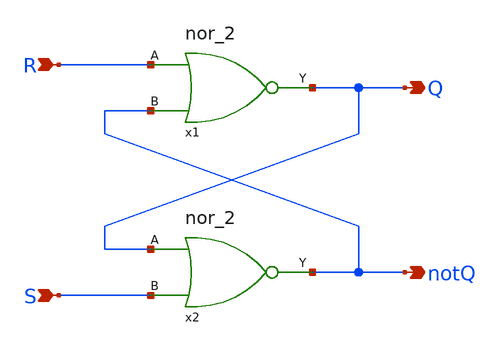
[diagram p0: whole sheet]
** sch_path: Circuiti/latches_sch_sym/sr_latch.sch
**.subckt sr_latch R S Q notQ
*.ipin R
*.ipin S
*.opin Q
*.opin notQ
x1 R Q notQ nor_2
x2 Q notQ S nor_2
**.ends

* expanding   symbol:  /home/matteo/Documenti/tesi/Circuiti/logic_gates_sch_sym/nor_2.sym # of
*+ pins=3
** sym_path: Circuiti/logic_gates_sch_sym/nor_2.sym
** sch_path: Circuiti/logic_gates_sch_sym/nor_2.sch
.subckt nor_2 A Y B
*.opin Y
*.ipin A
*.ipin B
XM1 Y B GND GND sky130_fd_pr__nfet_01v8 L=0.45 W=1 nf=1 ad='int((nf+1)/2) * W/nf * 0.29' as='int((nf+2)/2) * W/nf * 0.29'
+ pd='2*int((nf+1)/2) * (W/nf + 0.29)' ps='2*int((nf+2)/2) * (W/nf + 0.29)' nrd='0.29 / W' nrs='0.29 / W'
+ sa=0 sb=0 sd=0 mult=1 m=1
XM3 Y B net1 VDD sky130_fd_pr__pfet_01v8 L=0.15 W=4.8 nf=1 ad='int((nf+1)/2) * W/nf * 0.29' as='int((nf+2)/2) * W/nf * 0.29'
+ pd='2*int((nf+1)/2) * (W/nf + 0.29)' ps='2*int((nf+2)/2) * (W/nf + 0.29)' nrd='0.29 / W' nrs='0.29 / W'
+ sa=0 sb=0 sd=0 mult=1 m=1
XM4 net1 A Vdd VDD sky130_fd_pr__pfet_01v8 L=0.15 W=4.8 nf=1 ad='int((nf+1)/2) * W/nf * 0.29' as='int((nf+2)/2) * W/nf * 0.29'
+ pd='2*int((nf+1)/2) * (W/nf + 0.29)' ps='2*int((nf+2)/2) * (W/nf + 0.29)' nrd='0.29 / W' nrs='0.29 / W'
+ sa=0 sb=0 sd=0 mult=1 m=1
XM2 Y A GND GND sky130_fd_pr__nfet_01v8 L=0.45 W=1 nf=1 ad='int((nf+1)/2) * W/nf * 0.29' as='int((nf+2)/2) * W/nf * 0.29'
+ pd='2*int((nf+1)/2) * (W/nf + 0.29)' ps='2*int((nf+2)/2) * (W/nf + 0.29)' nrd='0.29 / W' nrs='0.29 / W'
+ sa=0 sb=0 sd=0 mult=1 m=1
.ends

.GLOBAL Vdd
.GLOBAL GND
.end
